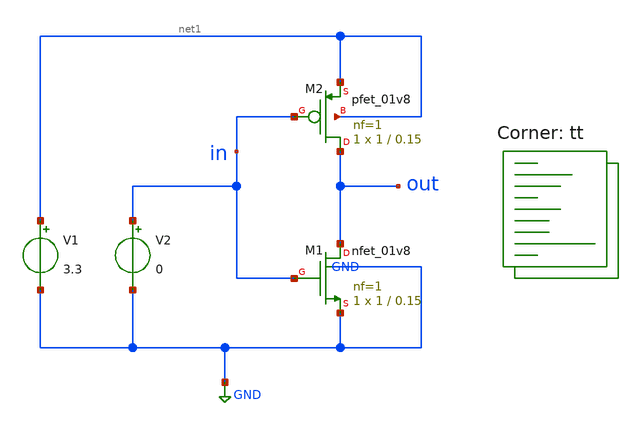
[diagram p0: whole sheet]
** sch_path: ringosi/untitled.sch
**.subckt untitled
XM1 out in GND GND sky130_fd_pr__nfet_01v8 L=0.15 W=1 nf=1 ad='int((nf+1)/2) * W/nf * 0.29' as='int((nf+2)/2) * W/nf * 0.29'
+ pd='2*int((nf+1)/2) * (W/nf + 0.29)' ps='2*int((nf+2)/2) * (W/nf + 0.29)' nrd='0.29 / W' nrs='0.29 / W'
+ sa=0 sb=0 sd=0 mult=1 m=1
XM2 out in net1 net1 sky130_fd_pr__pfet_01v8 L=0.15 W=1 nf=1 ad='int((nf+1)/2) * W/nf * 0.29' as='int((nf+2)/2) * W/nf * 0.29'
+ pd='2*int((nf+1)/2) * (W/nf + 0.29)' ps='2*int((nf+2)/2) * (W/nf + 0.29)' nrd='0.29 / W' nrs='0.29 / W'
+ sa=0 sb=0 sd=0 mult=1 m=1
V1 net1 GND 3.3
V2 in GND 0
**** begin user architecture code
.lib $::SKYWATER_MODELS/sky130.lib.spice tt


.control
dc V2 0 3.3 0.0115
plot out in
.endc


**** end user architecture code
**.ends
.GLOBAL GND
.end
